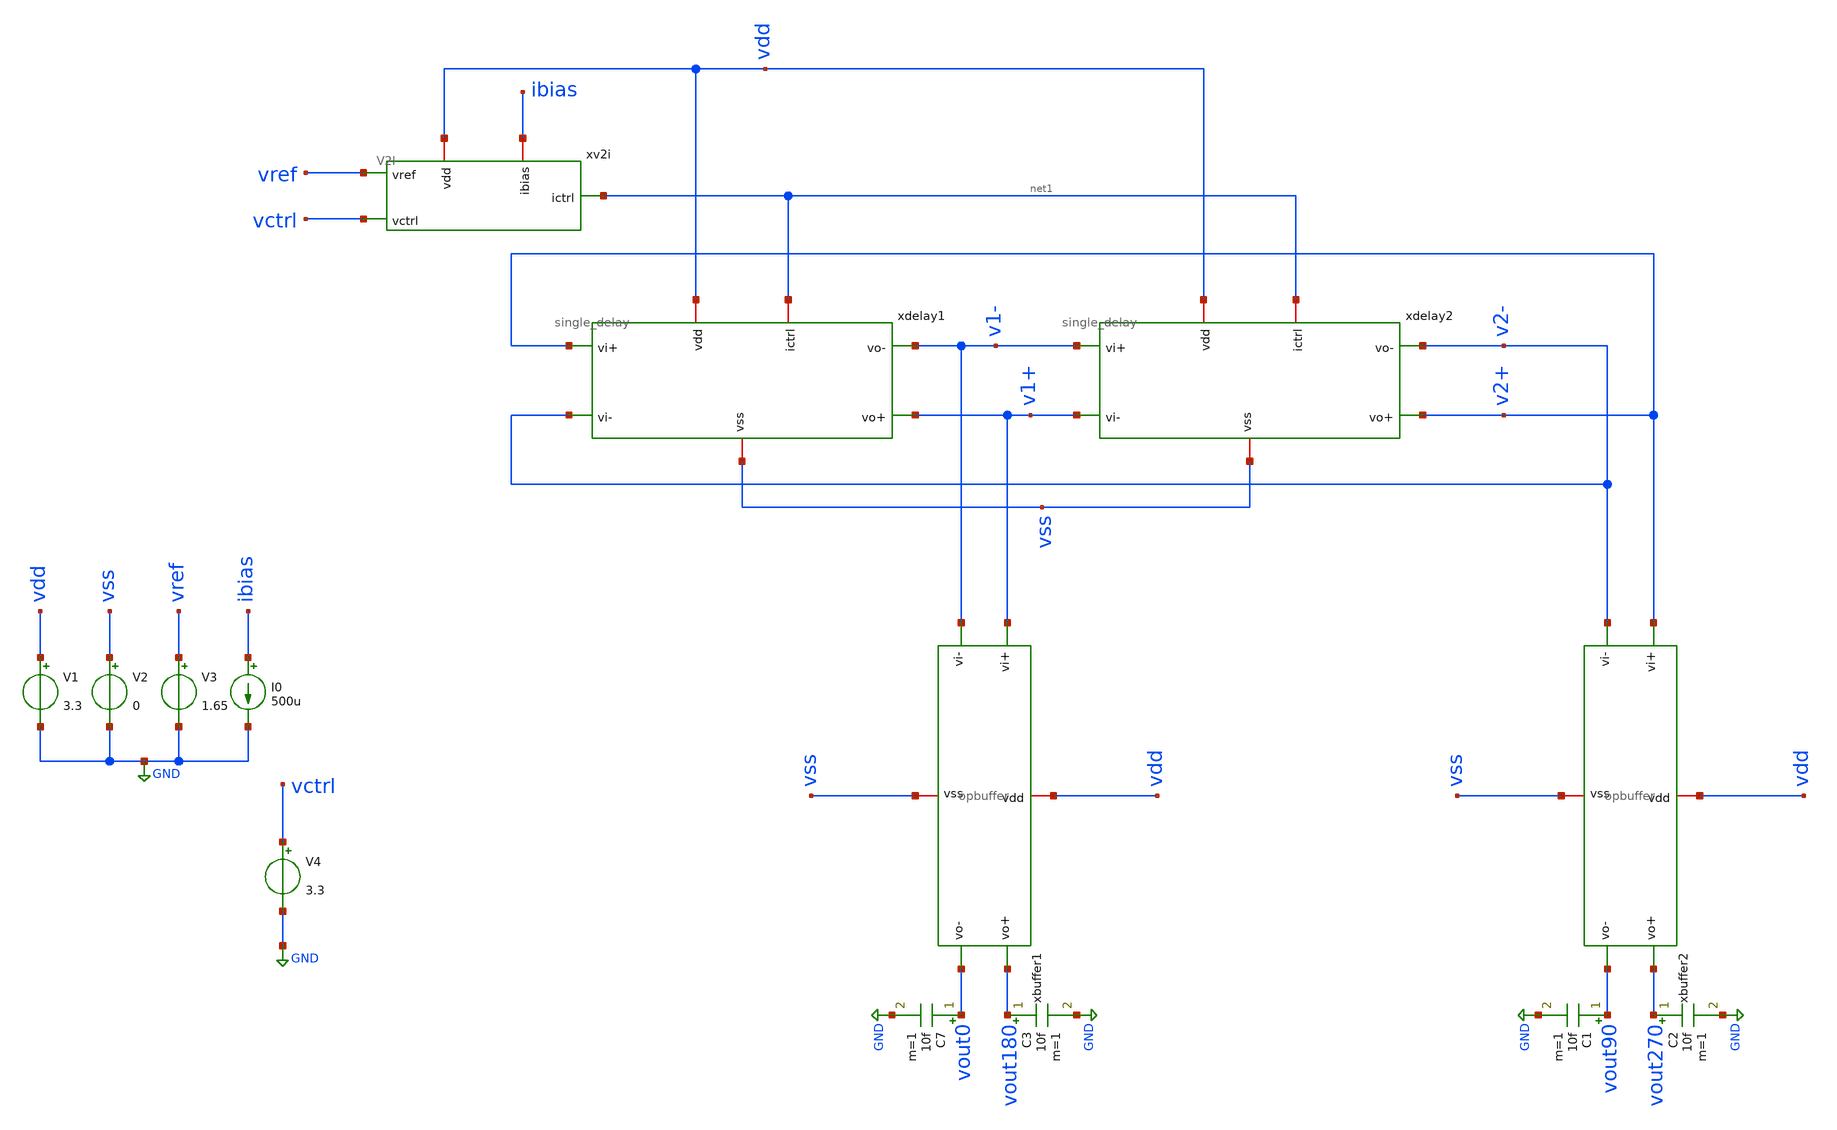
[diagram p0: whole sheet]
** sch_path: xschem/tb.sch
**.subckt tb
xdelay1 net1 vdd v2+ v2- v1- v1+ vss single_delay
xdelay2 net1 vdd v1- v1+ v2- v2+ vss single_delay
xv2i vdd net1 vref vctrl ibias V2I
xbuffer2 vdd vss v2+ vout270 vout90 v2- opbuffer
V1 vdd GND 3.3
V2 vss GND 0
V3 vref GND 1.65
I0 ibias GND 500u
V4 vctrl GND 3.3
xbuffer1 vdd vss v1+ vout180 vout0 v1- opbuffer
C7 vout0 GND 10f m=1
C1 vout90 GND 10f m=1
C2 vout270 GND 10f m=1
C3 vout180 GND 10f m=1
**** begin user architecture code

.include $::180MCU_MODELS/design.ngspice
.lib $::180MCU_MODELS/sm141064.ngspice typical
.lib $::180MCU_MODELS/sm141064.ngspice res_typical



.control
let start_v = 0.5
let stop_v  = 3.3
let step_v  = 0.05

let vctrl = start_v

let v_sweep = unitvec(57)
let freq_results = unitvec(57)
let i = 0

dowhile vctrl <= stop_v
	alter @V4[DC] = vctrl
	tran 10p 50n
	meas tran t1 WHEN v(vout0)=1.65 FALL=10
	meas tran t2 WHEN v(vout0)=1.65 FALL=11
	let freq = 1 / (t2 - t1)
	let v_sweep[i] = $&vctrl
	let freq_results[i] = freq
	print freq
	let vctrl = vctrl + step_v
	let i = i + 1
	reset
end
set nolegend
print freq_results
.endc


**** end user architecture code
**.ends

* expanding   symbol:  single_delay.sym # of pins=7
** sym_path: xschem/single_delay.sym
** sch_path: xschem/single_delay.sch
.subckt single_delay ictrl vdd vi+ vi- vo- vo+ vss
*.iopin ictrl
*.iopin vss
*.iopin vdd
*.ipin vi+
*.ipin vi-
*.opin vo-
*.opin vo+
XM1 vo- vi+ ictrl vdd pfet_03v3 L=0.28u W=6.48u nf=2 ad='int((nf+1)/2) * W/nf * 0.18u' as='int((nf+2)/2) * W/nf * 0.18u'
+ pd='2*int((nf+1)/2) * (W/nf + 0.18u)' ps='2*int((nf+2)/2) * (W/nf + 0.18u)' nrd='0.18u / W' nrs='0.18u / W'
+ sa=0 sb=0 sd=0 m=1
XM2 vo- vo+ ictrl vdd pfet_03v3 L=0.28u W=4.32u nf=2 ad='int((nf+1)/2) * W/nf * 0.18u' as='int((nf+2)/2) * W/nf * 0.18u'
+ pd='2*int((nf+1)/2) * (W/nf + 0.18u)' ps='2*int((nf+2)/2) * (W/nf + 0.18u)' nrd='0.18u / W' nrs='0.18u / W'
+ sa=0 sb=0 sd=0 m=1
XM3 vo+ vo- ictrl vdd pfet_03v3 L=0.28u W=4.32u nf=2 ad='int((nf+1)/2) * W/nf * 0.18u' as='int((nf+2)/2) * W/nf * 0.18u'
+ pd='2*int((nf+1)/2) * (W/nf + 0.18u)' ps='2*int((nf+2)/2) * (W/nf + 0.18u)' nrd='0.18u / W' nrs='0.18u / W'
+ sa=0 sb=0 sd=0 m=1
XM4 vo+ vi- ictrl vdd pfet_03v3 L=0.28u W=6.48u nf=2 ad='int((nf+1)/2) * W/nf * 0.18u' as='int((nf+2)/2) * W/nf * 0.18u'
+ pd='2*int((nf+1)/2) * (W/nf + 0.18u)' ps='2*int((nf+2)/2) * (W/nf + 0.18u)' nrd='0.18u / W' nrs='0.18u / W'
+ sa=0 sb=0 sd=0 m=1
XM5 vo- vi+ vss vss nfet_03v3 L=0.28u W=2.16u nf=2 ad='int((nf+1)/2) * W/nf * 0.18u' as='int((nf+2)/2) * W/nf * 0.18u'
+ pd='2*int((nf+1)/2) * (W/nf + 0.18u)' ps='2*int((nf+2)/2) * (W/nf + 0.18u)' nrd='0.18u / W' nrs='0.18u / W'
+ sa=0 sb=0 sd=0 m=1
XM6 vo- vo+ vss vss nfet_03v3 L=0.28u W=1.44u nf=2 ad='int((nf+1)/2) * W/nf * 0.18u' as='int((nf+2)/2) * W/nf * 0.18u'
+ pd='2*int((nf+1)/2) * (W/nf + 0.18u)' ps='2*int((nf+2)/2) * (W/nf + 0.18u)' nrd='0.18u / W' nrs='0.18u / W'
+ sa=0 sb=0 sd=0 m=1
XM7 vo+ vo- vss vss nfet_03v3 L=0.28u W=1.44u nf=2 ad='int((nf+1)/2) * W/nf * 0.18u' as='int((nf+2)/2) * W/nf * 0.18u'
+ pd='2*int((nf+1)/2) * (W/nf + 0.18u)' ps='2*int((nf+2)/2) * (W/nf + 0.18u)' nrd='0.18u / W' nrs='0.18u / W'
+ sa=0 sb=0 sd=0 m=1
XM8 vo+ vi- vss vss nfet_03v3 L=0.28u W=2.16u nf=2 ad='int((nf+1)/2) * W/nf * 0.18u' as='int((nf+2)/2) * W/nf * 0.18u'
+ pd='2*int((nf+1)/2) * (W/nf + 0.18u)' ps='2*int((nf+2)/2) * (W/nf + 0.18u)' nrd='0.18u / W' nrs='0.18u / W'
+ sa=0 sb=0 sd=0 m=1
.ends


* expanding   symbol:  V2I.sym # of pins=5
** sym_path: xschem/V2I.sym
** sch_path: xschem/V2I.sch
.subckt V2I vdd ictrl vref vctrl ibias
*.iopin vdd
*.iopin ibias
*.ipin vref
*.ipin vctrl
*.opin ictrl
XM17 net1 vctrl ibias ibias nfet_03v3 L=0.28u W=2.5u nf=5 ad='int((nf+1)/2) * W/nf * 0.18u' as='int((nf+2)/2) * W/nf * 0.18u'
+ pd='2*int((nf+1)/2) * (W/nf + 0.18u)' ps='2*int((nf+2)/2) * (W/nf + 0.18u)' nrd='0.18u / W' nrs='0.18u / W'
+ sa=0 sb=0 sd=0 m=1
XM18 net2 vref ibias ibias nfet_03v3 L=0.28u W=2.5u nf=5 ad='int((nf+1)/2) * W/nf * 0.18u' as='int((nf+2)/2) * W/nf * 0.18u'
+ pd='2*int((nf+1)/2) * (W/nf + 0.18u)' ps='2*int((nf+2)/2) * (W/nf + 0.18u)' nrd='0.18u / W' nrs='0.18u / W'
+ sa=0 sb=0 sd=0 m=1
XM19 net1 net1 vdd vdd pfet_03v3 L=0.5u W=10u nf=5 ad='int((nf+1)/2) * W/nf * 0.18u' as='int((nf+2)/2) * W/nf * 0.18u'
+ pd='2*int((nf+1)/2) * (W/nf + 0.18u)' ps='2*int((nf+2)/2) * (W/nf + 0.18u)' nrd='0.18u / W' nrs='0.18u / W'
+ sa=0 sb=0 sd=0 m=1
XM20 net2 net2 vdd vdd pfet_03v3 L=0.5u W=10u nf=5 ad='int((nf+1)/2) * W/nf * 0.18u' as='int((nf+2)/2) * W/nf * 0.18u'
+ pd='2*int((nf+1)/2) * (W/nf + 0.18u)' ps='2*int((nf+2)/2) * (W/nf + 0.18u)' nrd='0.18u / W' nrs='0.18u / W'
+ sa=0 sb=0 sd=0 m=1
XM21 ictrl net2 vdd vdd pfet_03v3 L=0.5u W=20u nf=5 ad='int((nf+1)/2) * W/nf * 0.18u' as='int((nf+2)/2) * W/nf * 0.18u'
+ pd='2*int((nf+1)/2) * (W/nf + 0.18u)' ps='2*int((nf+2)/2) * (W/nf + 0.18u)' nrd='0.18u / W' nrs='0.18u / W'
+ sa=0 sb=0 sd=0 m=1
.ends


* expanding   symbol:  opbuffer.sym # of pins=6
** sym_path: xschem/opbuffer.sym
** sch_path: xschem/opbuffer.sch
.subckt opbuffer vdd vss vi+ vo+ vo- vi-
*.iopin vdd
*.iopin vss
*.ipin vi+
*.ipin vi-
*.opin vo+
*.opin vo-
XM38 vo+ net1 vdd vdd pfet_03v3 L=0.28u W=12u nf=1 ad='int((nf+1)/2) * W/nf * 0.18u' as='int((nf+2)/2) * W/nf * 0.18u'
+ pd='2*int((nf+1)/2) * (W/nf + 0.18u)' ps='2*int((nf+2)/2) * (W/nf + 0.18u)' nrd='0.18u / W' nrs='0.18u / W'
+ sa=0 sb=0 sd=0 m=1
XM39 vo+ net1 vss vss nfet_03v3 L=0.28u W=5.3u nf=1 ad='int((nf+1)/2) * W/nf * 0.18u' as='int((nf+2)/2) * W/nf * 0.18u'
+ pd='2*int((nf+1)/2) * (W/nf + 0.18u)' ps='2*int((nf+2)/2) * (W/nf + 0.18u)' nrd='0.18u / W' nrs='0.18u / W'
+ sa=0 sb=0 sd=0 m=1
XM40 vo- net2 vdd vdd pfet_03v3 L=0.28u W=12u nf=1 ad='int((nf+1)/2) * W/nf * 0.18u' as='int((nf+2)/2) * W/nf * 0.18u'
+ pd='2*int((nf+1)/2) * (W/nf + 0.18u)' ps='2*int((nf+2)/2) * (W/nf + 0.18u)' nrd='0.18u / W' nrs='0.18u / W'
+ sa=0 sb=0 sd=0 m=1
XM41 vo- net2 vss vss nfet_03v3 L=0.28u W=5.3u nf=1 ad='int((nf+1)/2) * W/nf * 0.18u' as='int((nf+2)/2) * W/nf * 0.18u'
+ pd='2*int((nf+1)/2) * (W/nf + 0.18u)' ps='2*int((nf+2)/2) * (W/nf + 0.18u)' nrd='0.18u / W' nrs='0.18u / W'
+ sa=0 sb=0 sd=0 m=1
XM42 vo- vo+ vdd vdd pfet_03v3 L=0.28u W=0.9u nf=1 ad='int((nf+1)/2) * W/nf * 0.18u' as='int((nf+2)/2) * W/nf * 0.18u'
+ pd='2*int((nf+1)/2) * (W/nf + 0.18u)' ps='2*int((nf+2)/2) * (W/nf + 0.18u)' nrd='0.18u / W' nrs='0.18u / W'
+ sa=0 sb=0 sd=0 m=1
XM43 vo- vo+ vss vss nfet_03v3 L=0.28u W=0.4u nf=1 ad='int((nf+1)/2) * W/nf * 0.18u' as='int((nf+2)/2) * W/nf * 0.18u'
+ pd='2*int((nf+1)/2) * (W/nf + 0.18u)' ps='2*int((nf+2)/2) * (W/nf + 0.18u)' nrd='0.18u / W' nrs='0.18u / W'
+ sa=0 sb=0 sd=0 m=1
XM44 vo+ vo- vdd vdd pfet_03v3 L=0.28u W=0.9u nf=1 ad='int((nf+1)/2) * W/nf * 0.18u' as='int((nf+2)/2) * W/nf * 0.18u'
+ pd='2*int((nf+1)/2) * (W/nf + 0.18u)' ps='2*int((nf+2)/2) * (W/nf + 0.18u)' nrd='0.18u / W' nrs='0.18u / W'
+ sa=0 sb=0 sd=0 m=1
XM45 vo+ vo- vss vss nfet_03v3 L=0.28u W=0.4u nf=1 ad='int((nf+1)/2) * W/nf * 0.18u' as='int((nf+2)/2) * W/nf * 0.18u'
+ pd='2*int((nf+1)/2) * (W/nf + 0.18u)' ps='2*int((nf+2)/2) * (W/nf + 0.18u)' nrd='0.18u / W' nrs='0.18u / W'
+ sa=0 sb=0 sd=0 m=1
XM24 net1 net3 vdd vdd pfet_03v3 L=0.28u W=0.9u nf=1 ad='int((nf+1)/2) * W/nf * 0.18u' as='int((nf+2)/2) * W/nf * 0.18u'
+ pd='2*int((nf+1)/2) * (W/nf + 0.18u)' ps='2*int((nf+2)/2) * (W/nf + 0.18u)' nrd='0.18u / W' nrs='0.18u / W'
+ sa=0 sb=0 sd=0 m=1
XM25 net1 net3 vss vss nfet_03v3 L=0.28u W=0.4u nf=1 ad='int((nf+1)/2) * W/nf * 0.18u' as='int((nf+2)/2) * W/nf * 0.18u'
+ pd='2*int((nf+1)/2) * (W/nf + 0.18u)' ps='2*int((nf+2)/2) * (W/nf + 0.18u)' nrd='0.18u / W' nrs='0.18u / W'
+ sa=0 sb=0 sd=0 m=1
C2 vi+ net3 10f m=1
XM1 net2 net4 vdd vdd pfet_03v3 L=0.28u W=0.9u nf=1 ad='int((nf+1)/2) * W/nf * 0.18u' as='int((nf+2)/2) * W/nf * 0.18u'
+ pd='2*int((nf+1)/2) * (W/nf + 0.18u)' ps='2*int((nf+2)/2) * (W/nf + 0.18u)' nrd='0.18u / W' nrs='0.18u / W'
+ sa=0 sb=0 sd=0 m=1
XM2 net2 net4 vss vss nfet_03v3 L=0.28u W=0.4u nf=1 ad='int((nf+1)/2) * W/nf * 0.18u' as='int((nf+2)/2) * W/nf * 0.18u'
+ pd='2*int((nf+1)/2) * (W/nf + 0.18u)' ps='2*int((nf+2)/2) * (W/nf + 0.18u)' nrd='0.18u / W' nrs='0.18u / W'
+ sa=0 sb=0 sd=0 m=1
C1 vi- net4 10f m=1
XR1 net3 net1 vdd ppolyf_u_2k r_width=1u r_length=30u m=1
XR2 net4 net2 vdd ppolyf_u_2k r_width=1u r_length=30u m=1
.ends

.GLOBAL GND
.end
